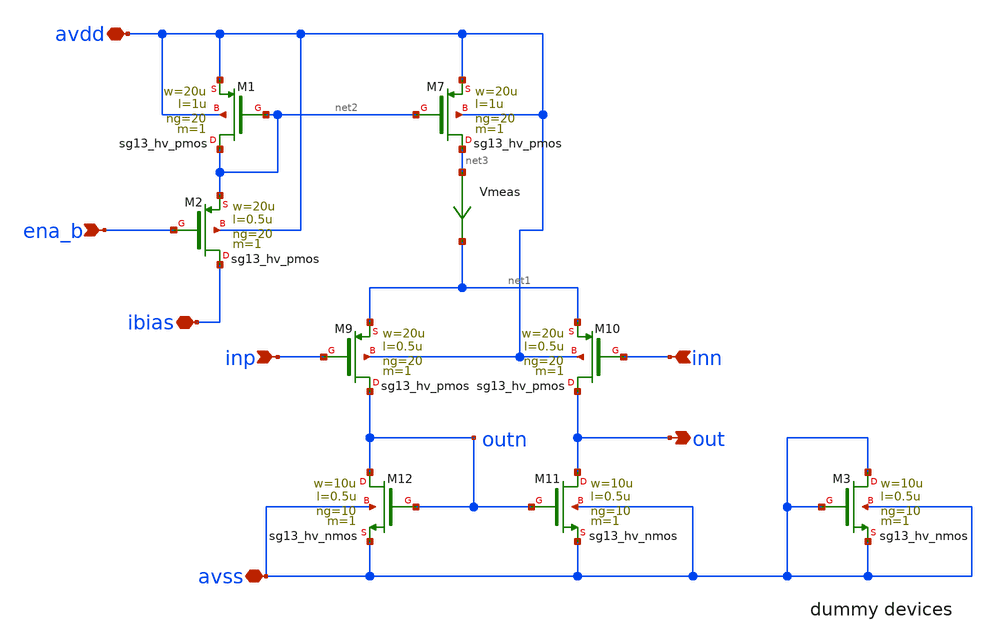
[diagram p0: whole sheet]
** sch_path: xschem/p_amp_large.sch
**.subckt p_amp_large avdd avss ena_b inp inn out ibias
*.iopin avdd
*.iopin avss
*.ipin ena_b
*.ipin inp
*.ipin inn
*.opin out
*.iopin ibias
XM7 net3 net2 avdd avdd sg13_hv_pmos w=20u l=1u ng=20 m=1 mm_ok=1
XM9 outn inp net1 avdd sg13_hv_pmos w=20u l=0.5u ng=20 m=1 mm_ok=1
XM10 out inn net1 avdd sg13_hv_pmos w=20u l=0.5u ng=20 m=1 mm_ok=1
XM11 out outn avss avss sg13_hv_nmos w=10u l=0.5u ng=10 m=1 mm_ok=1
XM12 outn outn avss avss sg13_hv_nmos w=10u l=0.5u ng=10 m=1 mm_ok=1
XM1 net2 net2 avdd avdd sg13_hv_pmos w=20u l=1u ng=20 m=1 mm_ok=1
XM2 ibias ena_b net2 avdd sg13_hv_pmos w=20u l=0.5u ng=20 m=1 mm_ok=1
Vmeas net3 net1 0
.save i(vmeas)
XM3 avss avss avss avss sg13_hv_nmos w=10u l=0.5u ng=10 m=1 mm_ok=1
**.ends
.end
